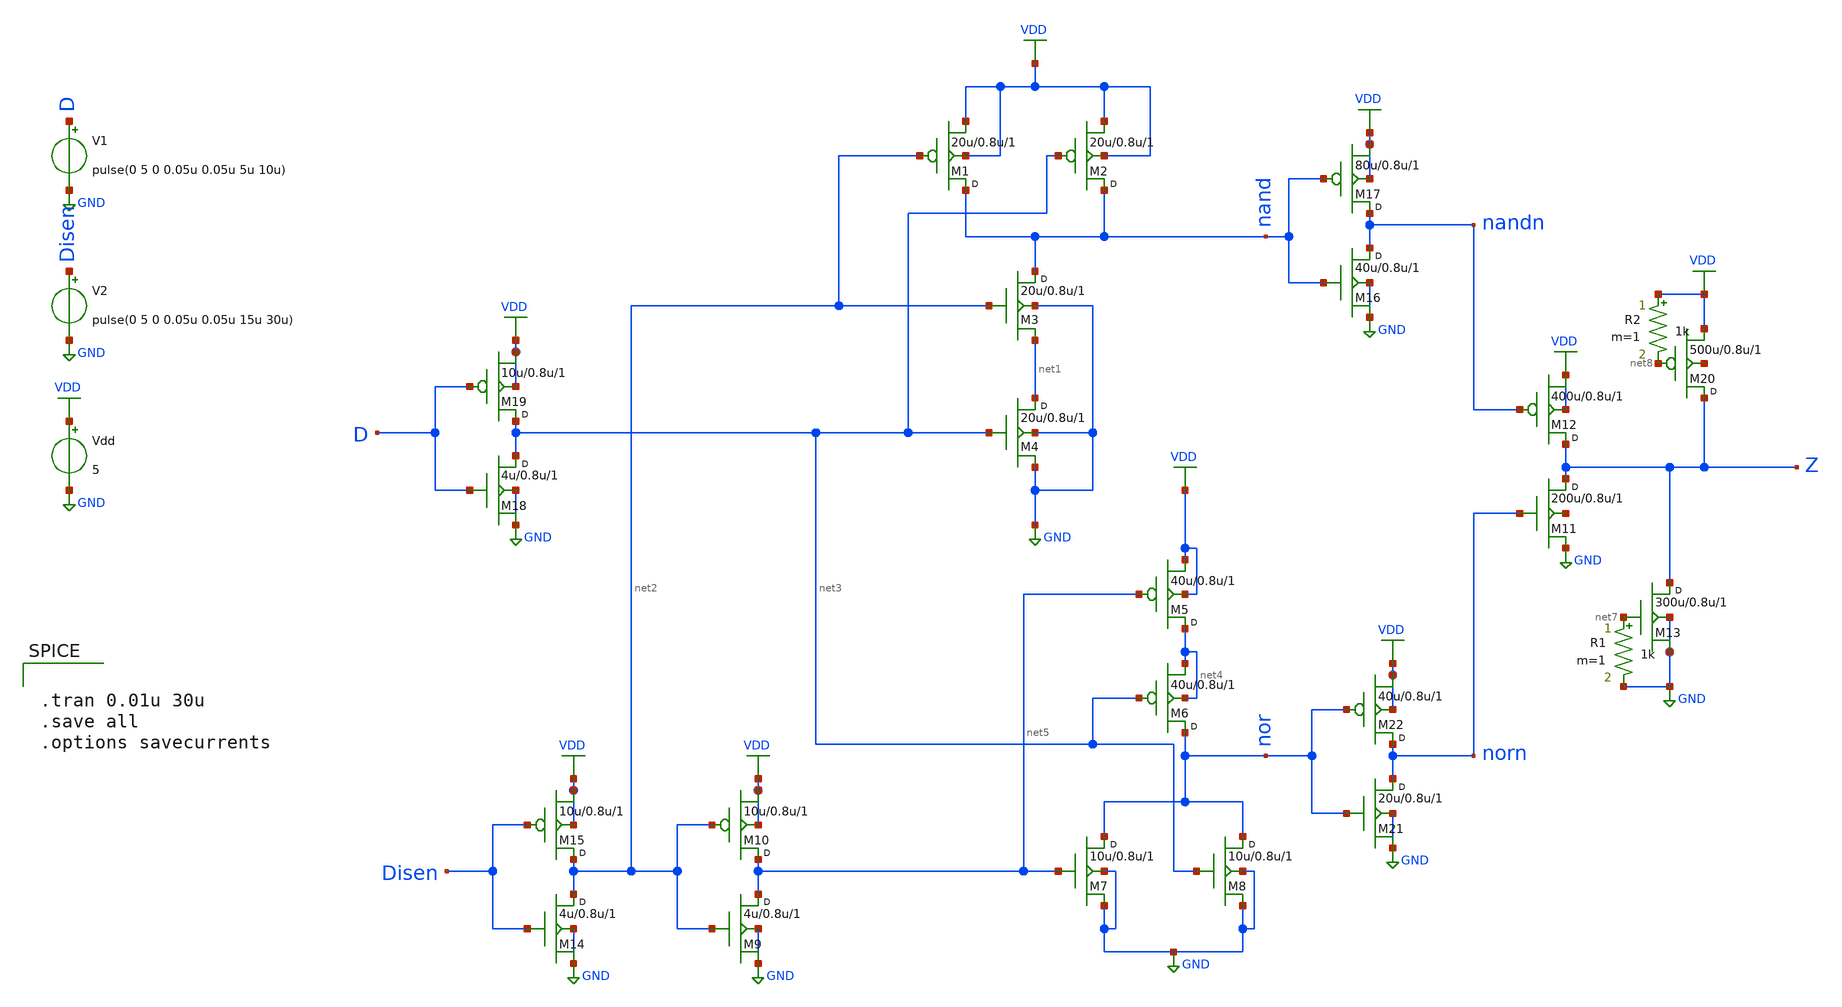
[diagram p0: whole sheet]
** sch_path: cells/out_pad/out_pad.sch
**.subckt out_pad
M3 nand net2 net1 GND nmos w=20u l=0.8u m=1
M4 net1 net3 GND GND nmos w=20u l=0.8u m=1
M1 nand net2 VDD VDD pmos w=20u l=0.8u m=1
M2 nand net3 VDD VDD pmos w=20u l=0.8u m=1
M5 net4 net5 VDD VDD pmos w=40u l=0.8u m=1
M6 nor net3 net4 net4 pmos w=40u l=0.8u m=1
M7 nor net5 GND GND nmos w=10u l=0.8u m=1
M8 nor net3 GND GND nmos w=10u l=0.8u m=1
M9 net5 net2 GND GND nmos w=4u l=0.8u m=1
M10 net5 net2 VDD VDD pmos w=10u l=0.8u m=1
M11 Z norn GND net6 nmos w=200u l=0.8u m=1
M12 Z nandn VDD VDD pmos w=400u l=0.8u m=1
V1 D GND pulse(0 5 0 0.05u 0.05u 5u 10u)
V2 Disen GND pulse(0 5 0 0.05u 0.05u 15u 30u)
Vdd VDD GND 5
M13 Z net7 GND GND nmos w=300u l=0.8u m=1
M14 net2 Disen GND GND nmos w=4u l=0.8u m=1
M15 net2 Disen VDD VDD pmos w=10u l=0.8u m=1
M18 net3 D GND GND nmos w=4u l=0.8u m=1
M19 net3 D VDD VDD pmos w=10u l=0.8u m=1
R1 net7 GND 1k m=1
M20 Z net8 VDD net9 pmos w=500u l=0.8u m=1
R2 VDD net8 1k m=1
M16 nandn nand GND GND nmos w=40u l=0.8u m=1
M17 nandn nand VDD VDD pmos w=80u l=0.8u m=1
M21 norn nor GND GND nmos w=20u l=0.8u m=1
M22 norn nor VDD VDD pmos w=40u l=0.8u m=1
**** begin user architecture code


.tran 0.01u 30u
.save all
.options savecurrents



.model nmos nmos level=49 version=3.3.0
.model pmos pmos level=49 version=3.3.0

**** end user architecture code
**.ends
.GLOBAL VDD
.GLOBAL GND
.end
